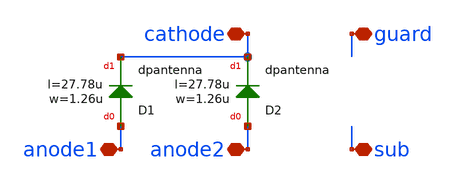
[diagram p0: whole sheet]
** sch_path: libs.tech/xschem/hm_stdcells/sg13g2_DCPDiode_noptap.sch
**.subckt sg13g2_DCPDiode_noptap anode2 cathode guard anode1 sub
*.iopin anode2
*.iopin cathode
*.iopin guard
*.iopin anode1
*.iopin sub
XD1 anode1 cathode dpantenna l=27.78u w=1.26u
XD2 anode2 cathode dpantenna l=27.78u w=1.26u
**.ends
.end
